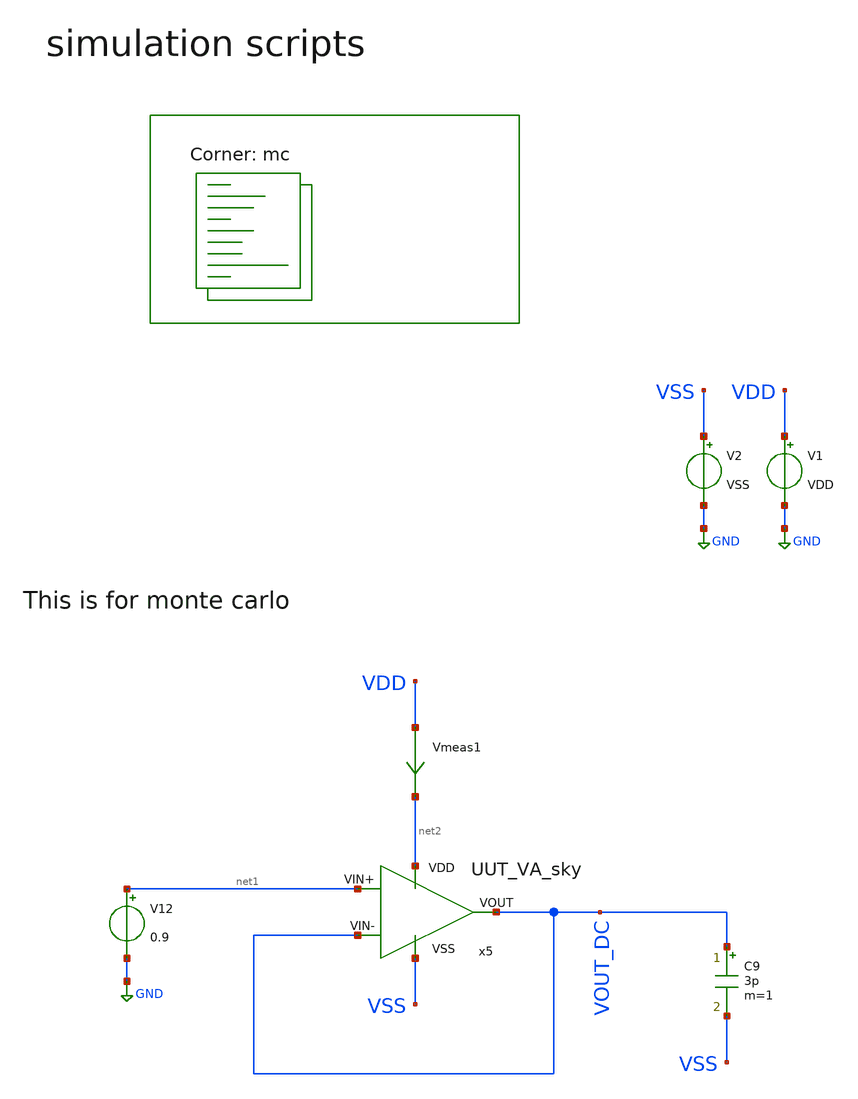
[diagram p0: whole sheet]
** sch_path: Learning/single_ended_amplifiers/Design_and_Analysis_of_Two-Stage_CMOS_Operational_Amplifier_for_Fluorescence_Signal_Processing_sky130_5V/amplifier_design/OTA_mc_dc_tb.sch
**.subckt OTA_mc_dc_tb
V1 VDD GND VDD
V2 VSS GND VSS
Vmeas1 VDD net2 0
.save i(vmeas1)
x5 net2 VSS VOUT_DC net1 VOUT_DC UUT_VA_sky
C9 VOUT_DC VSS 3p m=1
V12 net1 GND 0.9
**** begin user architecture code
.lib $::SKYWATER_MODELS/sky130.lib.spice mc

.Temp 27
.param VDD = 5
.param VSS = 0
.param CL = 3p
.param mc_mm_switch = 1

.control

	save all
	dc V12 0 1.8 0.01
	plot v(VOUT_DC)
	wrdata mc_dc.csv v(VOUT_DC) i(Vmeas1)
.endc

**** end user architecture code
**.ends

* expanding   symbol:  Sky130A/UUT_sky/UUT_VA_sky.sym # of pins=5
** sym_path: my_ip/LIB/Sky130A/UUT_sky/UUT_VA_sky.sym
** sch_path: my_ip/LIB/Sky130A/UUT_sky/UUT_VA_sky.sch
.subckt UUT_VA_sky VDD VSS VIN- VIN+ VOUT
*.iopin VDD
*.iopin VSS
*.iopin VIN-
*.iopin VIN+
*.iopin VOUT
x1 VDD VSS VIN+ VIN- VOUT A001
.ends

.GLOBAL GND
.end
